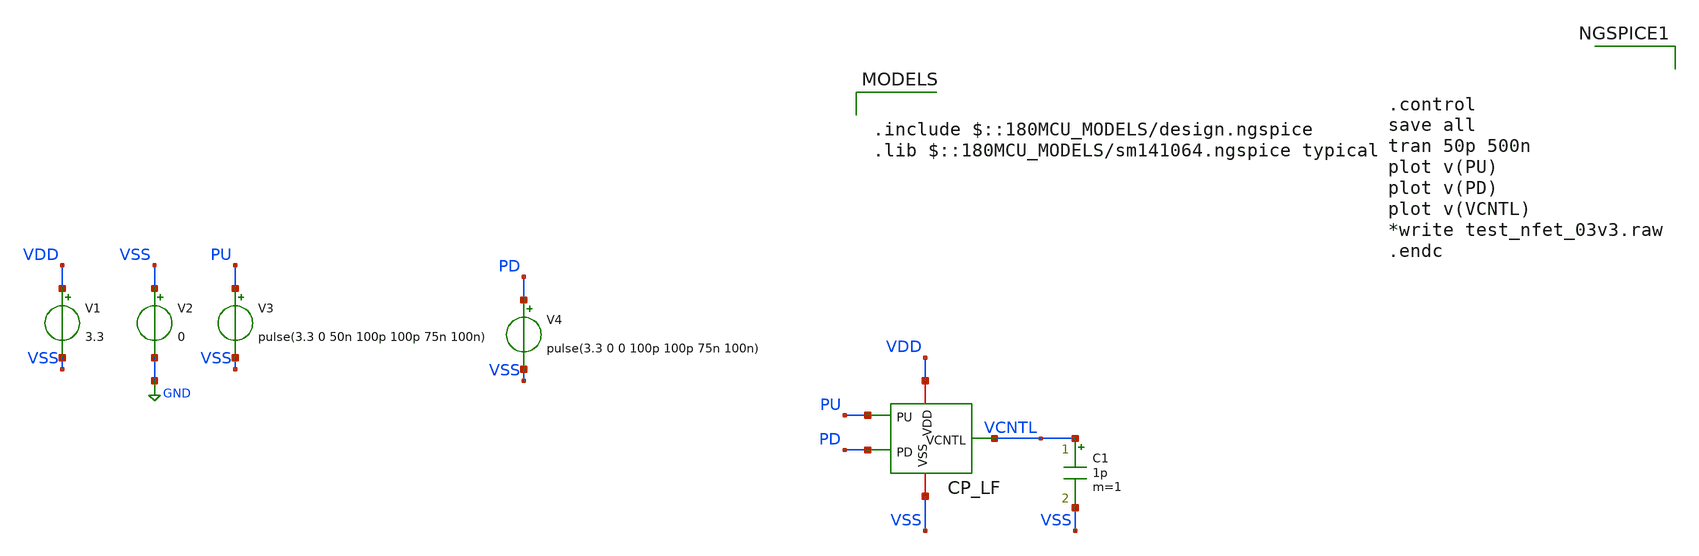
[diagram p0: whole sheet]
** sch_path: Clock_Generator_PAKISTAN_02/xschem/CP_LF_test.sch
**.subckt CP_LF_test
V1 VDD VSS 3.3
V2 VSS GND 0
V3 PU VSS pulse(3.3 0 50n 100p 100p 75n 100n)
V4 PD VSS pulse(3.3 0 0 100p 100p 75n 100n)
C1 VCNTL VSS 1p m=1
x1 VSS PU VCNTL PD VDD CP_LF
**** begin user architecture code

.include $::180MCU_MODELS/design.ngspice
.lib $::180MCU_MODELS/sm141064.ngspice typical




.control
save all
tran 50p 500n
plot v(PU)
plot v(PD)
plot v(VCNTL)
*write test_nfet_03v3.raw
.endc


**** end user architecture code
**.ends
.GLOBAL GND
.end
